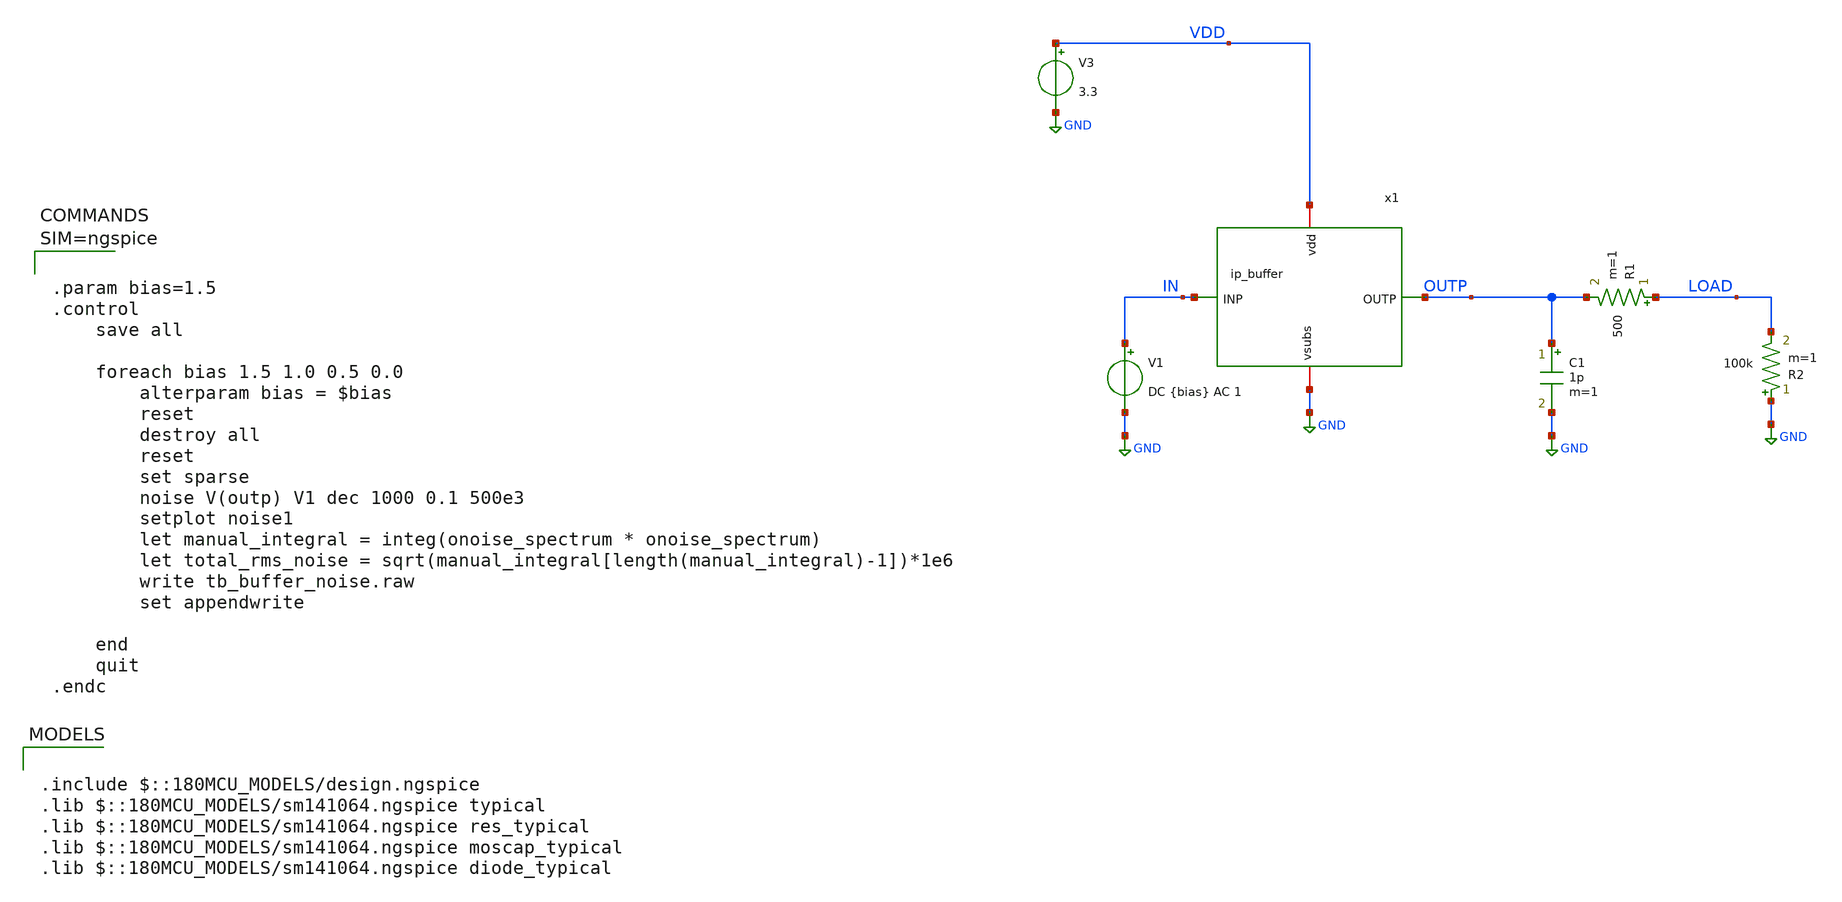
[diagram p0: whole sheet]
** sch_path: xschem/tb_buffer_noise.sch
**.subckt tb_buffer_noise
x1 VDD OUTP IN GND ip_buffer
V3 VDD GND 3.3
V1 IN GND DC {bias} AC 1
R1 LOAD OUTP 500 m=1
C1 OUTP GND 1p m=1
R2 GND LOAD 100k m=1
**** begin user architecture code

.include $::180MCU_MODELS/design.ngspice
.lib $::180MCU_MODELS/sm141064.ngspice typical
.lib $::180MCU_MODELS/sm141064.ngspice res_typical
.lib $::180MCU_MODELS/sm141064.ngspice moscap_typical
.lib $::180MCU_MODELS/sm141064.ngspice diode_typical




.param bias=1.5
.control
	save all

	foreach bias 1.5 1.0 0.5 0.0
		alterparam bias = $bias
		reset
		destroy all
		reset
		set sparse
		noise V(outp) V1 dec 1000 0.1 500e3
		setplot noise1
		let manual_integral = integ(onoise_spectrum * onoise_spectrum)
		let total_rms_noise = sqrt(manual_integral[length(manual_integral)-1])*1e6
		write tb_buffer_noise.raw
		set appendwrite

	end
	quit
.endc



**** end user architecture code
**.ends

* expanding   symbol:  ip_buffer.sym # of pins=4
** sym_path: xschem/ip_buffer.sym
** sch_path: xschem/ip_buffer.sch
.subckt ip_buffer vdd OUTP INP vsubs
*.iopin vsubs
*.iopin vdd
*.ipin INP
*.opin OUTP
XM1 vsubs INP OUTP OUTP pfet_06v0 L=1u W=10u nf=1 ad='int((nf+1)/2) * W/nf * 0.18u' as='int((nf+2)/2) * W/nf * 0.18u'
+ pd='2*int((nf+1)/2) * (W/nf + 0.18u)' ps='2*int((nf+2)/2) * (W/nf + 0.18u)' nrd='0.18u / W' nrs='0.18u / W'
+ sa=0 sb=0 sd=0 m=15
Vmeas net1 net2 0
XM4 OUTP net1 vdd vdd pfet_06v0 L=2u W=10u nf=1 ad='int((nf+1)/2) * W/nf * 0.18u' as='int((nf+2)/2) * W/nf * 0.18u'
+ pd='2*int((nf+1)/2) * (W/nf + 0.18u)' ps='2*int((nf+2)/2) * (W/nf + 0.18u)' nrd='0.18u / W' nrs='0.18u / W'
+ sa=0 sb=0 sd=0 m=5
XM2 net1 net1 vdd vdd pfet_06v0 L=2u W=10u nf=1 ad='int((nf+1)/2) * W/nf * 0.18u' as='int((nf+2)/2) * W/nf * 0.18u'
+ pd='2*int((nf+1)/2) * (W/nf + 0.18u)' ps='2*int((nf+2)/2) * (W/nf + 0.18u)' nrd='0.18u / W' nrs='0.18u / W'
+ sa=0 sb=0 sd=0 m=4
XR1 net4 net2 vsubs ppolyf_u_1k_6p0 r_width=1e-6 r_length=6e-6 m=1
XR2 net3 net4 vsubs ppolyf_u_1k_6p0 r_width=1e-6 r_length=6e-6 m=1
XR3 net5 net3 vsubs ppolyf_u_1k_6p0 r_width=1e-6 r_length=6e-6 m=1
XR4 vsubs net5 vsubs ppolyf_u_1k_6p0 r_width=1e-6 r_length=6e-6 m=1
.ends

.GLOBAL GND
.end
